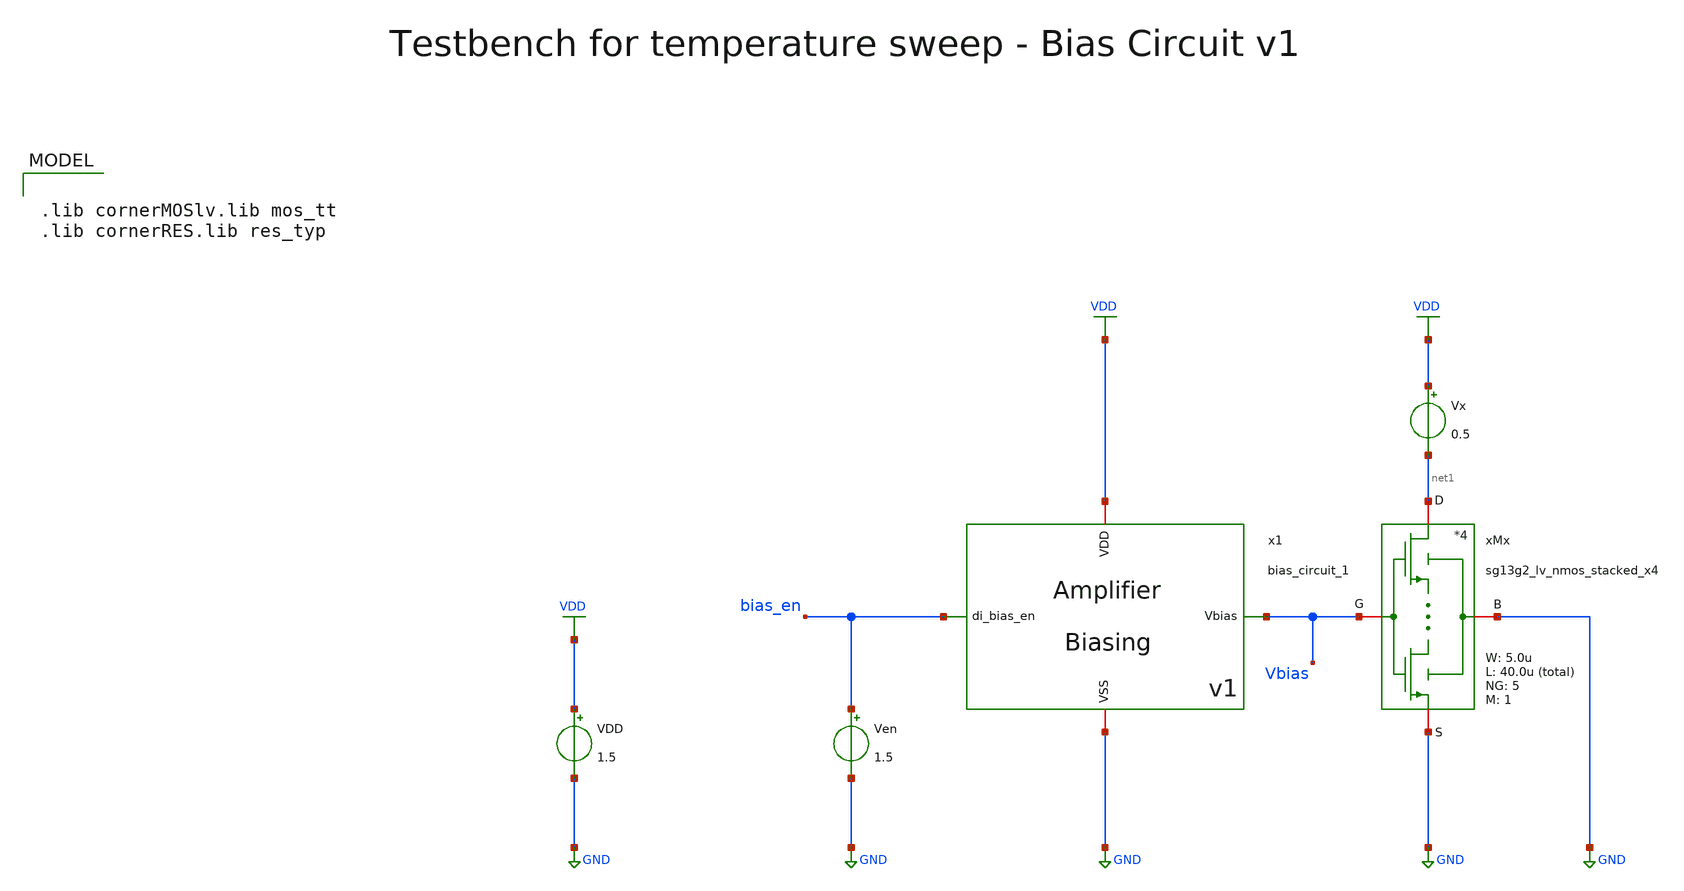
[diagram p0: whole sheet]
** sch_path: SG13G2_ATBS-ADC-main/xschem/bio_amplifier/amplifier_core/bias_circuit/bias_circuit_1/testbenches/bias_circuit_1_tb_temp.sch
**.subckt bias_circuit_1_tb_temp
Ven bias_en GND 1.5
VDD VDD GND 1.5
x1 bias_en Vbias VDD GND bias_circuit_1
xMx net1 Vbias GND GND sg13g2_lv_nmos_stacked_x4 W_N=5.0u L_N=40.0u NG_N=5 M_N=1
Vx VDD net1 0.5
**** begin user architecture code

.lib cornerMOSlv.lib mos_tt
.lib cornerRES.lib res_typ



.param temp=27
.options savecurrents reltol=1e-3 abstol=1e-15 gmin=1e-15
.control
save all

* User Constants
* Commercial Temperature Range
let Troom = 27
let Tmin = 0
let Tmax = 70
let Tstep = 1

* Operating Point Analysis
op
remzerovec
write bias_circuit_1_tb_temp.raw
set appendwrite

* Temperature Sweep
dc temp $&Tmin $&Tmax $&Tstep
remzerovec
write bias_circuit_1_tb_temp.raw

* Plotting
plot v(Vbias)
plot i(Vx)

* Measurements of Vbias
meas dc Vbias_Troom FIND Vbias at=Troom
meas dc Vbias_Tmin FIND Vbias at=Tmin
meas dc Vbias_Tmax FIND Vbias at=Tmax

* Calculate ppm/°C
let dVbias = Vbias_Tmax - Vbias_Tmin
print dVbias

let dT = Tmax - Tmin
print dT

let ppm_deg = (dVbias / Vbias_Troom) * (1e6 / dT)
print ppm_deg

* Measurements of Ix
meas dc Ix_Troom FIND i(Vx) at=Troom
meas dc Ix_Tmin FIND i(Vx) at=Tmin
meas dc Ix_Tmax FIND i(Vx) at=Tmax

* Calculate ppm/°C
let dIx = Ix_Tmax - Ix_Tmin
print dIx

let ppm_deg = (dIx / Ix_Troom) * (1e6 / dT)
print ppm_deg

* Write Data
set wr_vecnames
set wr_singlescale
let Ix=i(Vx)
wrdata /foss/designs/SG13G2_ATBS-ADC-main/python/plot_simulations/data/bias_circuit_1_tb_temp.txt
+ v(Vbias) v(Ix)

*quit
.endc

**** end user architecture code
**.ends
.GLOBAL GND
.GLOBAL VDD
.end
